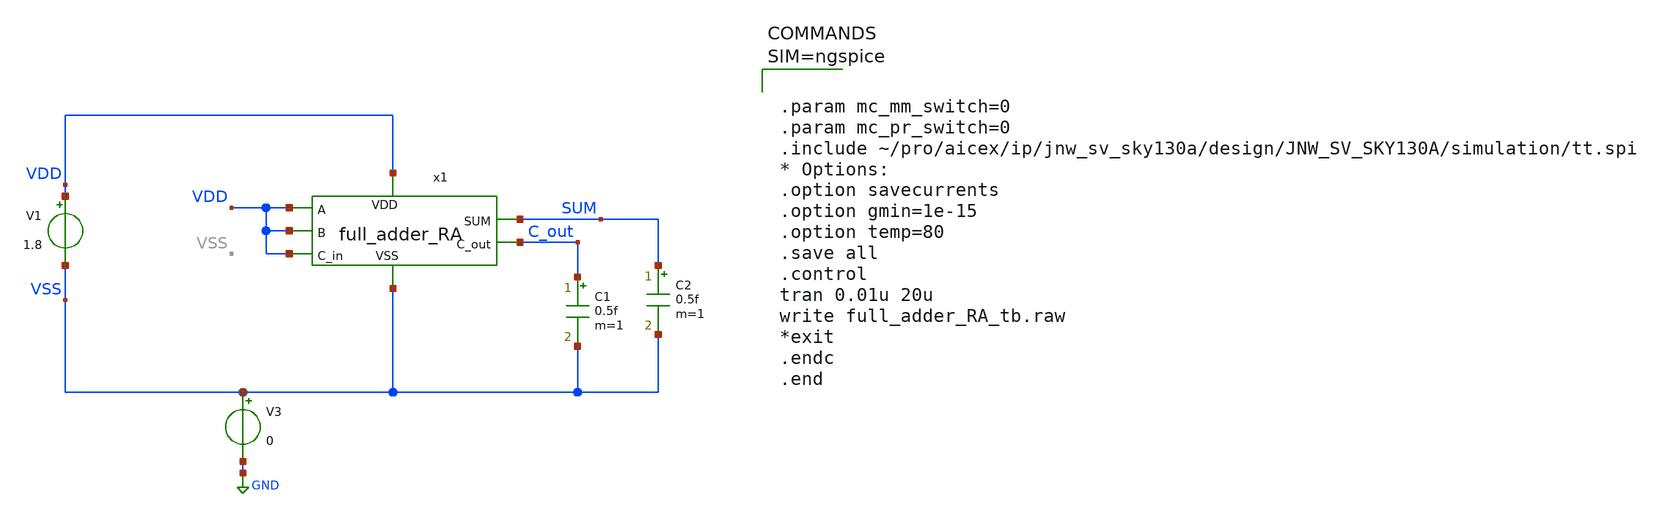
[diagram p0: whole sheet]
** sch_path: design/JNW_GR07_SKY130A/full_adder_RA_tb.sch
**.subckt full_adder_RA_tb
x1 VDD VSS SUM VDD C_out VDD VDD full_adder_RA
V3 VSS GND 0
V1 VDD VSS 1.8
C1 C_out VSS 0.5f m=1
C2 SUM VSS 0.5f m=1
**** begin user architecture code



.param mc_mm_switch=0
.param mc_pr_switch=0
.include ~/pro/aicex/ip/jnw_sv_sky130a/design/JNW_SV_SKY130A/simulation/tt.spi
* Options:
.option savecurrents
.option gmin=1e-15
.option temp=80
.save all
.control
tran 0.01u 20u
write full_adder_RA_tb.raw
*exit
.endc
.end



**** end user architecture code
**.ends
.GLOBAL GND
.end
